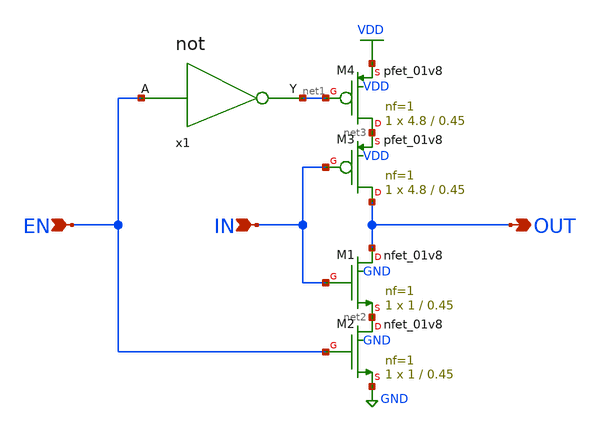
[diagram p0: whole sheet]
** sch_path: Circuiti/memories/tri_state_inv.sch
**.subckt tri_state_inv EN IN OUT
*.ipin EN
*.ipin IN
*.opin OUT
XM1 OUT IN net2 GND sky130_fd_pr__nfet_01v8 L=0.45 W=1 nf=1 ad='int((nf+1)/2) * W/nf * 0.29' as='int((nf+2)/2) * W/nf * 0.29'
+ pd='2*int((nf+1)/2) * (W/nf + 0.29)' ps='2*int((nf+2)/2) * (W/nf + 0.29)' nrd='0.29 / W' nrs='0.29 / W'
+ sa=0 sb=0 sd=0 mult=1 m=1
XM2 net2 EN GND GND sky130_fd_pr__nfet_01v8 L=0.45 W=1 nf=1 ad='int((nf+1)/2) * W/nf * 0.29' as='int((nf+2)/2) * W/nf * 0.29'
+ pd='2*int((nf+1)/2) * (W/nf + 0.29)' ps='2*int((nf+2)/2) * (W/nf + 0.29)' nrd='0.29 / W' nrs='0.29 / W'
+ sa=0 sb=0 sd=0 mult=1 m=1
XM3 OUT IN net3 VDD sky130_fd_pr__pfet_01v8 L=0.45 W=4.8 nf=1 ad='int((nf+1)/2) * W/nf * 0.29' as='int((nf+2)/2) * W/nf * 0.29'
+ pd='2*int((nf+1)/2) * (W/nf + 0.29)' ps='2*int((nf+2)/2) * (W/nf + 0.29)' nrd='0.29 / W' nrs='0.29 / W'
+ sa=0 sb=0 sd=0 mult=1 m=1
XM4 net3 net1 VDD VDD sky130_fd_pr__pfet_01v8 L=0.45 W=4.8 nf=1 ad='int((nf+1)/2) * W/nf * 0.29' as='int((nf+2)/2) * W/nf * 0.29'
+ pd='2*int((nf+1)/2) * (W/nf + 0.29)' ps='2*int((nf+2)/2) * (W/nf + 0.29)' nrd='0.29 / W' nrs='0.29 / W'
+ sa=0 sb=0 sd=0 mult=1 m=1
x1 EN net1 not
**.ends

* expanding   symbol:  /home/matteo/Documenti/tesi/Circuiti/logic_gates_sch_sym/not.sym # of pins=2
** sym_path: Circuiti/logic_gates_sch_sym/not.sym
** sch_path: Circuiti/logic_gates_sch_sym/not.sch
.subckt not A Y
*.ipin A
*.opin Y
XM1 Y A GND GND sky130_fd_pr__nfet_01v8 L=0.45 W=1 nf=1 ad='int((nf+1)/2) * W/nf * 0.29' as='int((nf+2)/2) * W/nf * 0.29'
+ pd='2*int((nf+1)/2) * (W/nf + 0.29)' ps='2*int((nf+2)/2) * (W/nf + 0.29)' nrd='0.29 / W' nrs='0.29 / W'
+ sa=0 sb=0 sd=0 mult=1 m=1
XM2 Y A Vdd VDD sky130_fd_pr__pfet_01v8 L=0.45 W=4.8 nf=1 ad='int((nf+1)/2) * W/nf * 0.29' as='int((nf+2)/2) * W/nf * 0.29'
+ pd='2*int((nf+1)/2) * (W/nf + 0.29)' ps='2*int((nf+2)/2) * (W/nf + 0.29)' nrd='0.29 / W' nrs='0.29 / W'
+ sa=0 sb=0 sd=0 mult=1 m=1
.ends

.GLOBAL VDD
.GLOBAL GND
.GLOBAL Vdd
.end
